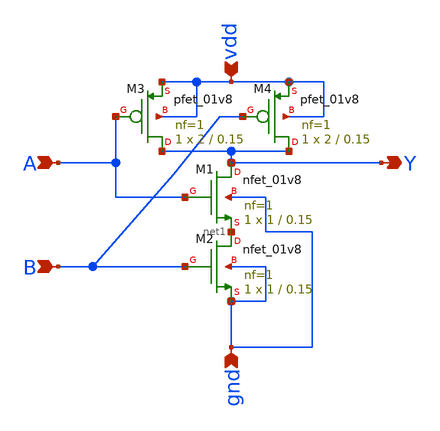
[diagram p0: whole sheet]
** sch_path: Circuit Files/Logic gate design using MOSFETS/gates/NAND_gate.sch
**.subckt NAND_gate A B Y vdd gnd
*.ipin A
*.ipin B
*.opin Y
*.ipin vdd
*.ipin gnd
XM1 Y A net1 gnd sky130_fd_pr__nfet_01v8 L=0.15 W=1 nf=1 ad='int((nf+1)/2) * W/nf * 0.29' as='int((nf+2)/2) * W/nf * 0.29'
+ pd='2*int((nf+1)/2) * (W/nf + 0.29)' ps='2*int((nf+2)/2) * (W/nf + 0.29)' nrd='0.29 / W' nrs='0.29 / W'
+ sa=0 sb=0 sd=0 mult=1 m=1
XM2 net1 B gnd gnd sky130_fd_pr__nfet_01v8 L=0.15 W=1 nf=1 ad='int((nf+1)/2) * W/nf * 0.29' as='int((nf+2)/2) * W/nf * 0.29'
+ pd='2*int((nf+1)/2) * (W/nf + 0.29)' ps='2*int((nf+2)/2) * (W/nf + 0.29)' nrd='0.29 / W' nrs='0.29 / W'
+ sa=0 sb=0 sd=0 mult=1 m=1
XM3 Y A vdd vdd sky130_fd_pr__pfet_01v8 L=0.15 W=2 nf=1 ad='int((nf+1)/2) * W/nf * 0.29' as='int((nf+2)/2) * W/nf * 0.29'
+ pd='2*int((nf+1)/2) * (W/nf + 0.29)' ps='2*int((nf+2)/2) * (W/nf + 0.29)' nrd='0.29 / W' nrs='0.29 / W'
+ sa=0 sb=0 sd=0 mult=1 m=1
XM4 Y B vdd vdd sky130_fd_pr__pfet_01v8 L=0.15 W=2 nf=1 ad='int((nf+1)/2) * W/nf * 0.29' as='int((nf+2)/2) * W/nf * 0.29'
+ pd='2*int((nf+1)/2) * (W/nf + 0.29)' ps='2*int((nf+2)/2) * (W/nf + 0.29)' nrd='0.29 / W' nrs='0.29 / W'
+ sa=0 sb=0 sd=0 mult=1 m=1
**.ends
.end
